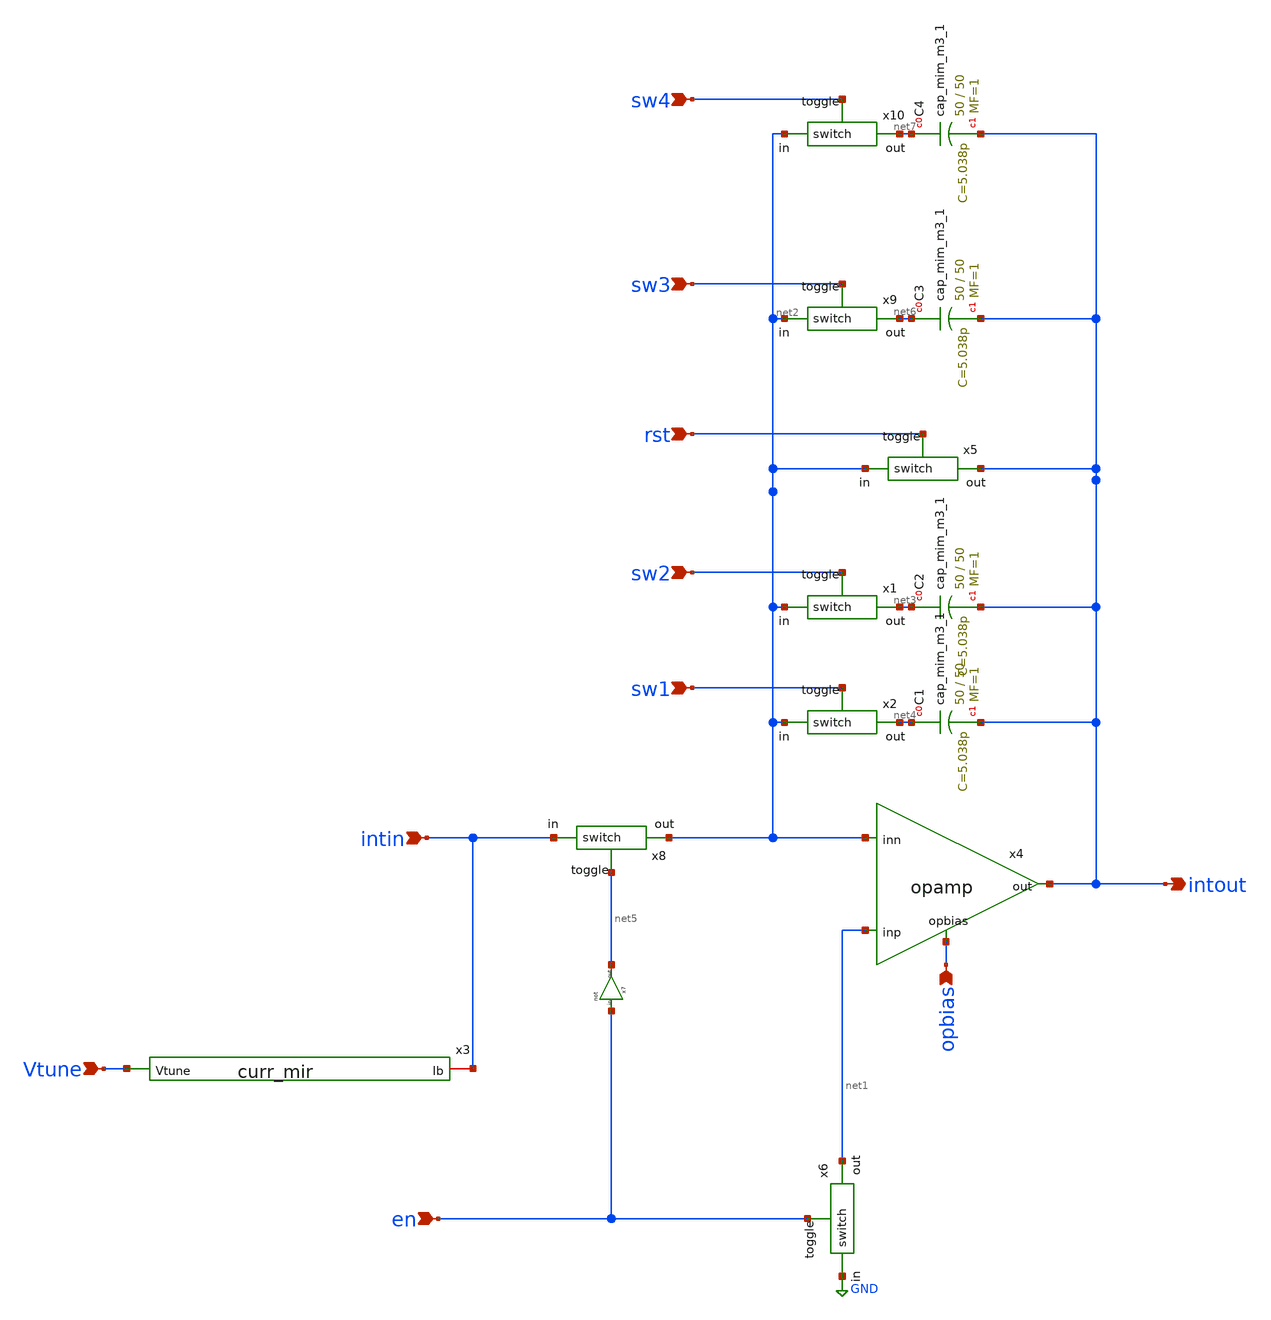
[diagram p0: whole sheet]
** sch_path: xschem/Integrator/integrator.sch
**.subckt integrator intin Vtune intout opbias sw1 sw2 rst en sw3 sw4
*.ipin intin
*.ipin Vtune
*.opin intout
*.ipin opbias
*.ipin sw1
*.ipin sw2
*.ipin rst
*.ipin en
*.ipin sw3
*.ipin sw4
XC1 net4 intout sky130_fd_pr__cap_mim_m3_1 W=50 L=50 MF=1 m=1
XC2 net3 intout sky130_fd_pr__cap_mim_m3_1 W=50 L=50 MF=1 m=1
x1 sw2 net3 net2 switch
x2 sw1 net4 net2 switch
x3 Vtune intin curr_mir
x4 opbias net1 net2 intout opamp
x5 rst intout net2 switch
x6 en net1 GND switch
x7 net5 en not
x8 net5 net2 intin switch
XC3 net6 intout sky130_fd_pr__cap_mim_m3_1 W=50 L=50 MF=1 m=1
x9 sw3 net6 net2 switch
XC4 net7 intout sky130_fd_pr__cap_mim_m3_1 W=50 L=50 MF=1 m=1
x10 sw4 net7 net2 switch
**.ends

* expanding   symbol:  switch/switch.sym # of pins=3
** sym_path: xschem/switch/switch.sym
** sch_path: xschem/switch/switch.sch
.subckt switch toggle out in
*.ipin toggle
*.ipin in
*.opin out
XM10 in net1 out out sky130_fd_pr__pfet_01v8_lvt L=3 W=200 nf=5 ad='int((5 + 1)/2) * 200 / 5 * 0.29'
+ as='int((5 + 2)/2) * 200 / 5 * 0.29' pd='2*int((5 + 1)/2) * (200 / 5 + 0.29)' ps='2*int((5 + 2)/2) * (200 / 5 + 0.29)'
+ nrd='0.29 / 200 ' nrs='0.29 / 200 ' sa=0 sb=0 sd=0 mult=1 m=1
XM1 in toggle out GND sky130_fd_pr__nfet_01v8_lvt L=3 W=200 nf=5 ad='int((5 + 1)/2) * 200 / 5 * 0.29'
+ as='int((5 + 2)/2) * 200 / 5 * 0.29' pd='2*int((5 + 1)/2) * (200 / 5 + 0.29)' ps='2*int((5 + 2)/2) * (200 / 5 + 0.29)'
+ nrd='0.29 / 200 ' nrs='0.29 / 200 ' sa=0 sb=0 sd=0 mult=1 m=1
x1 net1 toggle not
.ends


* expanding   symbol:  current_mirror/curr_mir.sym # of pins=2
** sym_path: xschem/current_mirror/curr_mir.sym
** sch_path: xschem/current_mirror/curr_mir.sch
.subckt curr_mir Vtune Ib
*.ipin Vtune
*.iopin Ib
XM1 net1 net1 GND GND sky130_fd_pr__nfet_01v8_lvt L=2 W=50 nf=1 ad='int((1 + 1)/2) * 50 / 1 * 0.29' as='int((1 + 2)/2) * 50 / 1 * 0.29'
+ pd='2*int((1 + 1)/2) * (50 / 1 + 0.29)' ps='2*int((1 + 2)/2) * (50 / 1 + 0.29)' nrd='0.29 / 50 ' nrs='0.29 / 50 '
+ sa=0 sb=0 sd=0 mult=1 m=1
XM2 Ib net1 GND GND sky130_fd_pr__nfet_01v8_lvt L=25 W=4 nf=1 ad='int((1 + 1)/2) * 4 / 1 * 0.29' as='int((1 + 2)/2) * 4 / 1 * 0.29'
+ pd='2*int((1 + 1)/2) * (4 / 1 + 0.29)' ps='2*int((1 + 2)/2) * (4 / 1 + 0.29)' nrd='0.29 / 4 ' nrs='0.29 / 4 '
+ sa=0 sb=0 sd=0 mult=1 m=1
XM10 net1 Vtune VDD VDD sky130_fd_pr__pfet_01v8_lvt L=10 W=10 nf=1 ad='int((1 + 1)/2) * 10 / 1 * 0.29'
+ as='int((1 + 2)/2) * 10 / 1 * 0.29' pd='2*int((1 + 1)/2) * (10 / 1 + 0.29)' ps='2*int((1 + 2)/2) * (10 / 1 + 0.29)'
+ nrd='0.29 / 10 ' nrs='0.29 / 10 ' sa=0 sb=0 sd=0 mult=1 m=1
.ends


* expanding   symbol:  opamp/opamp.sym # of pins=4
** sym_path: xschem/opamp/opamp.sym
** sch_path: xschem/opamp/opamp.sch
.subckt opamp opbias inp inn out
*.ipin inp
*.ipin inn
*.ipin opbias
*.opin out
XC1 net5 out sky130_fd_pr__cap_mim_m3_1 W=2 L=4 MF=1 m=1
XC2 out net4 sky130_fd_pr__cap_mim_m3_1 W=2 L=4 MF=1 m=1
XM26 net2 opbias VDD VDD sky130_fd_pr__pfet_01v8_lvt L=3 W=10 nf=4 ad='int((4 + 1)/2) * 10 / 4 * 0.29'
+ as='int((4 + 2)/2) * 10 / 4 * 0.29' pd='2*int((4 + 1)/2) * (10 / 4 + 0.29)' ps='2*int((4 + 2)/2) * (10 / 4 + 0.29)'
+ nrd='0.29 / 10 ' nrs='0.29 / 10 ' sa=0 sb=0 sd=0 mult=1 m=1
XM3 net1 net1 VDD VDD sky130_fd_pr__pfet_01v8_lvt L=3 W=10 nf=2 ad='int((2 + 1)/2) * 10 / 2 * 0.29' as='int((2 + 2)/2) * 10 / 2 * 0.29'
+ pd='2*int((2 + 1)/2) * (10 / 2 + 0.29)' ps='2*int((2 + 2)/2) * (10 / 2 + 0.29)' nrd='0.29 / 10 ' nrs='0.29 / 10 '
+ sa=0 sb=0 sd=0 mult=1 m=1
XM4 net5 net1 VDD VDD sky130_fd_pr__pfet_01v8_lvt L=3 W=10 nf=2 ad='int((2 + 1)/2) * 10 / 2 * 0.29' as='int((2 + 2)/2) * 10 / 2 * 0.29'
+ pd='2*int((2 + 1)/2) * (10 / 2 + 0.29)' ps='2*int((2 + 2)/2) * (10 / 2 + 0.29)' nrd='0.29 / 10 ' nrs='0.29 / 10 '
+ sa=0 sb=0 sd=0 mult=1 m=1
XM10 out net5 VDD VDD sky130_fd_pr__pfet_01v8_lvt L=3 W=100 nf=5 ad='int((5 + 1)/2) * 100 / 5 * 0.29'
+ as='int((5 + 2)/2) * 100 / 5 * 0.29' pd='2*int((5 + 1)/2) * (100 / 5 + 0.29)' ps='2*int((5 + 2)/2) * (100 / 5 + 0.29)'
+ nrd='0.29 / 100 ' nrs='0.29 / 100 ' sa=0 sb=0 sd=0 mult=1 m=1
XM14 net3 inn net2 net2 sky130_fd_pr__pfet_01v8_lvt L=3 W=15 nf=3 ad='int((3 + 1)/2) * 15 / 3 * 0.29'
+ as='int((3 + 2)/2) * 15 / 3 * 0.29' pd='2*int((3 + 1)/2) * (15 / 3 + 0.29)' ps='2*int((3 + 2)/2) * (15 / 3 + 0.29)'
+ nrd='0.29 / 15 ' nrs='0.29 / 15 ' sa=0 sb=0 sd=0 mult=1 m=1
XM15 net4 inp net2 net2 sky130_fd_pr__pfet_01v8_lvt L=3 W=15 nf=3 ad='int((3 + 1)/2) * 15 / 3 * 0.29'
+ as='int((3 + 2)/2) * 15 / 3 * 0.29' pd='2*int((3 + 1)/2) * (15 / 3 + 0.29)' ps='2*int((3 + 2)/2) * (15 / 3 + 0.29)'
+ nrd='0.29 / 15 ' nrs='0.29 / 15 ' sa=0 sb=0 sd=0 mult=1 m=1
XM17 out net4 GND GND sky130_fd_pr__nfet_01v8_lvt L=3 W=80 nf=5 ad='int((5 + 1)/2) * 80 / 5 * 0.29' as='int((5 + 2)/2) * 80 / 5 * 0.29'
+ pd='2*int((5 + 1)/2) * (80 / 5 + 0.29)' ps='2*int((5 + 2)/2) * (80 / 5 + 0.29)' nrd='0.29 / 80 ' nrs='0.29 / 80 '
+ sa=0 sb=0 sd=0 mult=1 m=1
XM19 net4 net3 GND GND sky130_fd_pr__nfet_01v8_lvt L=3 W=5 nf=1 ad='int((1 + 1)/2) * 5 / 1 * 0.29' as='int((1 + 2)/2) * 5 / 1 * 0.29'
+ pd='2*int((1 + 1)/2) * (5 / 1 + 0.29)' ps='2*int((1 + 2)/2) * (5 / 1 + 0.29)' nrd='0.29 / 5 ' nrs='0.29 / 5 '
+ sa=0 sb=0 sd=0 mult=1 m=1
XM20 net3 net3 GND GND sky130_fd_pr__nfet_01v8_lvt L=3 W=5 nf=1 ad='int((1 + 1)/2) * 5 / 1 * 0.29' as='int((1 + 2)/2) * 5 / 1 * 0.29'
+ pd='2*int((1 + 1)/2) * (5 / 1 + 0.29)' ps='2*int((1 + 2)/2) * (5 / 1 + 0.29)' nrd='0.29 / 5 ' nrs='0.29 / 5 '
+ sa=0 sb=0 sd=0 mult=1 m=1
XM2 net1 net4 GND GND sky130_fd_pr__nfet_01v8_lvt L=3 W=8 nf=1 ad='int((1 + 1)/2) * 8 / 1 * 0.29' as='int((1 + 2)/2) * 8 / 1 * 0.29'
+ pd='2*int((1 + 1)/2) * (8 / 1 + 0.29)' ps='2*int((1 + 2)/2) * (8 / 1 + 0.29)' nrd='0.29 / 8 ' nrs='0.29 / 8 '
+ sa=0 sb=0 sd=0 mult=1 m=1
XM5 net5 net3 GND GND sky130_fd_pr__nfet_01v8_lvt L=3 W=8 nf=1 ad='int((1 + 1)/2) * 8 / 1 * 0.29' as='int((1 + 2)/2) * 8 / 1 * 0.29'
+ pd='2*int((1 + 1)/2) * (8 / 1 + 0.29)' ps='2*int((1 + 2)/2) * (8 / 1 + 0.29)' nrd='0.29 / 8 ' nrs='0.29 / 8 '
+ sa=0 sb=0 sd=0 mult=1 m=1
.ends


* expanding   symbol:  not/not.sym # of pins=2
** sym_path: xschem/not/not.sym
** sch_path: xschem/not/not.sch
.subckt not out in
*.ipin in
*.opin out
XM10 out in VDD VDD sky130_fd_pr__pfet_01v8_lvt L=0.35 W=1 nf=1 ad='int((1 + 1)/2) * 1 / 1 * 0.29' as='int((1 + 2)/2) * 1 / 1 * 0.29'
+ pd='2*int((1 + 1)/2) * (1 / 1 + 0.29)' ps='2*int((1 + 2)/2) * (1 / 1 + 0.29)' nrd='0.29 / 1 ' nrs='0.29 / 1 '
+ sa=0 sb=0 sd=0 mult=1 m=1
XM1 out in GND GND sky130_fd_pr__nfet_01v8_lvt L=0.15 W=1 nf=1 ad='int((1 + 1)/2) * 1 / 1 * 0.29' as='int((1 + 2)/2) * 1 / 1 * 0.29'
+ pd='2*int((1 + 1)/2) * (1 / 1 + 0.29)' ps='2*int((1 + 2)/2) * (1 / 1 + 0.29)' nrd='0.29 / 1 ' nrs='0.29 / 1 '
+ sa=0 sb=0 sd=0 mult=1 m=1
.ends

.GLOBAL GND
.GLOBAL VDD
.end
